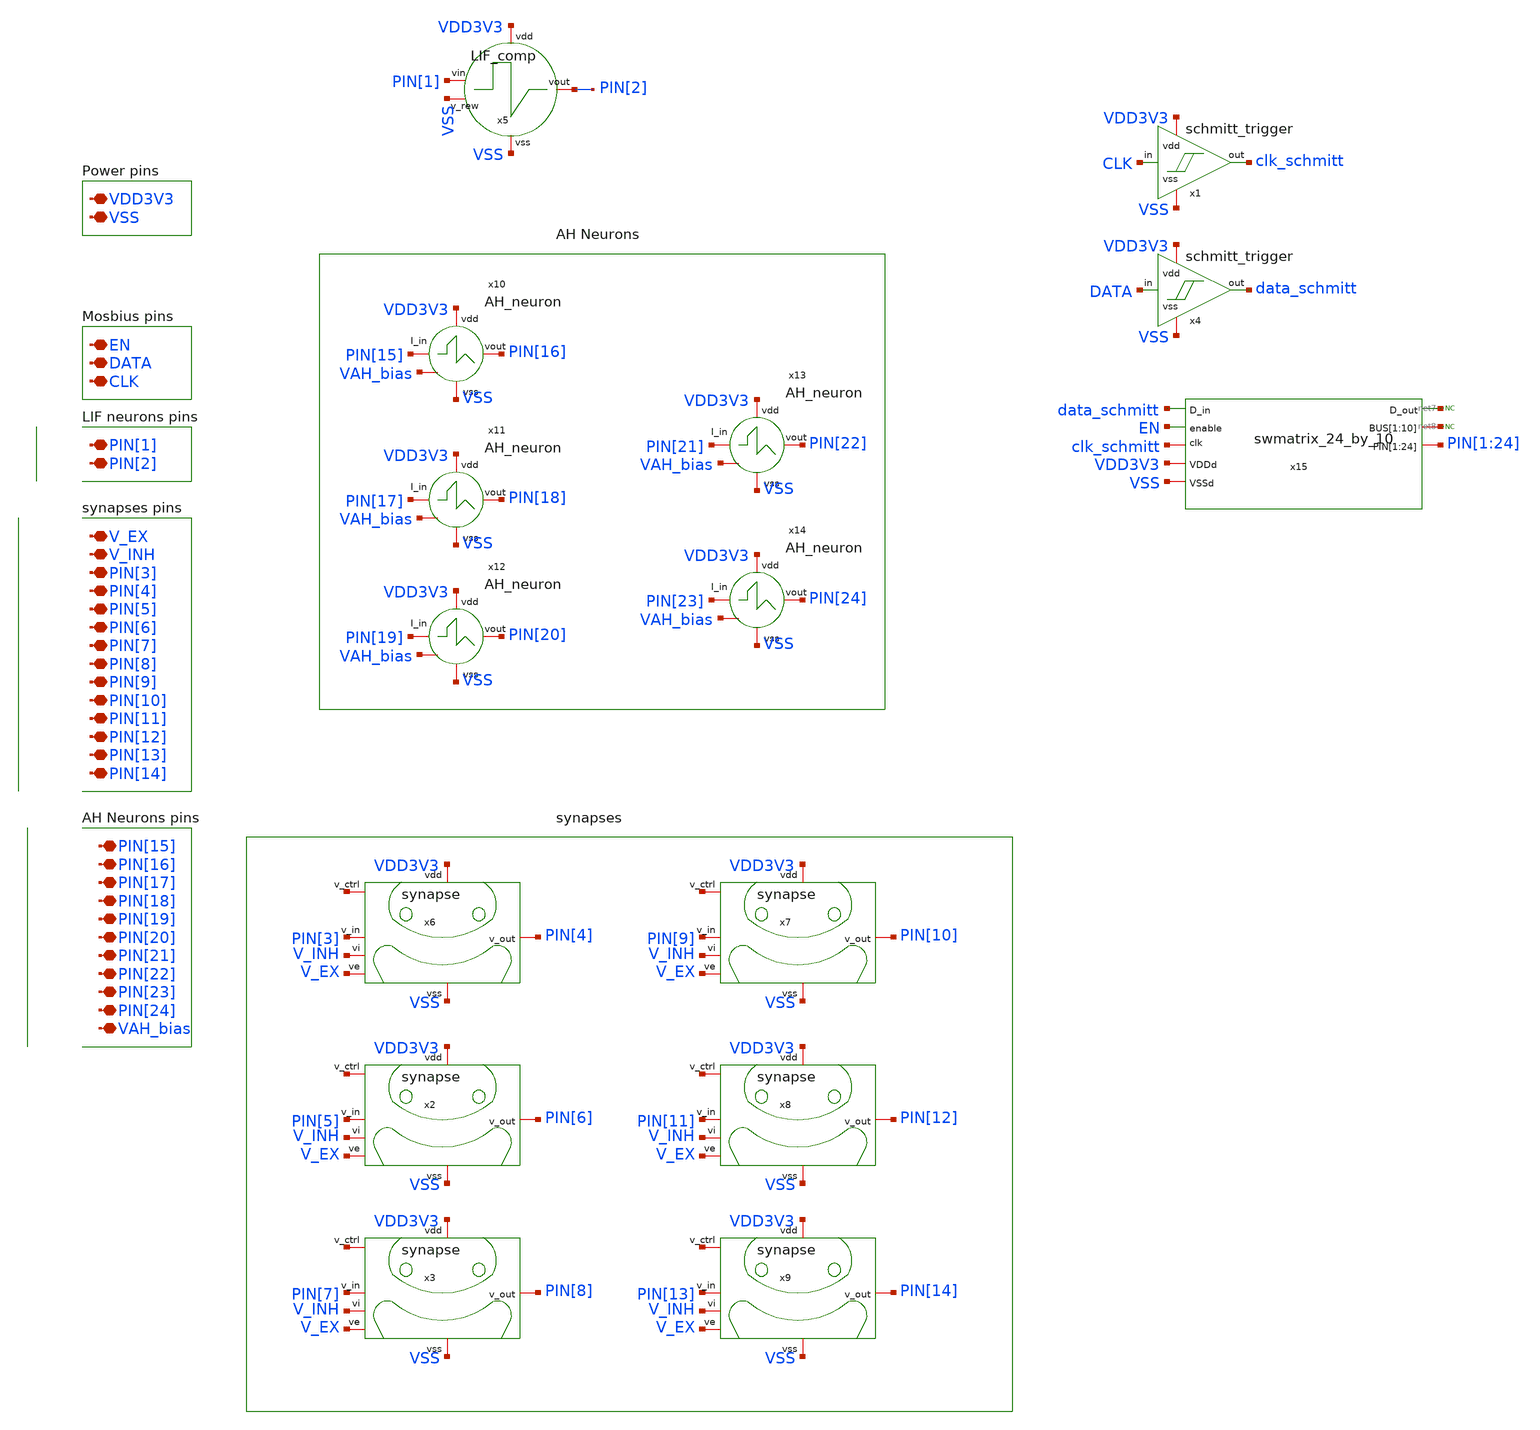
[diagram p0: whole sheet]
** sch_path: designs/klayout/layout_top/top.sch
**.subckt top PIN[15] PIN[16] PIN[17] PIN[18] PIN[19] PIN[20] PIN[21] PIN[22] VDD3V3 VSS PIN[1]
*+ PIN[2] V_EX V_INH PIN[3] PIN[4] PIN[5] PIN[6] PIN[7] PIN[8] EN DATA CLK PIN[23] PIN[24] PIN[9] PIN[10]
*+ PIN[11] PIN[12] PIN[13] PIN[14] VAH_bias
*.iopin PIN[15]
*.iopin PIN[16]
*.iopin PIN[17]
*.iopin PIN[18]
*.iopin PIN[19]
*.iopin PIN[20]
*.iopin PIN[21]
*.iopin PIN[22]
*.iopin VDD3V3
*.iopin VSS
*.iopin PIN[1]
*.iopin PIN[2]
*.iopin V_EX
*.iopin V_INH
*.iopin PIN[3]
*.iopin PIN[4]
*.iopin PIN[5]
*.iopin PIN[6]
*.iopin PIN[7]
*.iopin PIN[8]
*.iopin EN
*.iopin DATA
*.iopin CLK
*.iopin PIN[23]
*.iopin PIN[24]
*.iopin PIN[9]
*.iopin PIN[10]
*.iopin PIN[11]
*.iopin PIN[12]
*.iopin PIN[13]
*.iopin PIN[14]
*.iopin VAH_bias
x5 VDD3V3 VSS PIN[1] VSS PIN[2] LIF_comp
x6 VDD3V3 PIN[3] V_EX net1 PIN[4] V_INH VSS synapse
x2 VDD3V3 PIN[5] V_EX net2 PIN[6] V_INH VSS synapse
x3 VDD3V3 PIN[7] V_EX net3 PIN[8] V_INH VSS synapse
x7 VDD3V3 PIN[9] V_EX net4 PIN[10] V_INH VSS synapse
x8 VDD3V3 PIN[11] V_EX net5 PIN[12] V_INH VSS synapse
x9 VDD3V3 PIN[13] V_EX net6 PIN[14] V_INH VSS synapse
x10 VDD3V3 PIN[15] PIN[16] VSS VAH_bias AH_neuron
x11 VDD3V3 PIN[17] PIN[18] VSS VAH_bias AH_neuron
x12 VDD3V3 PIN[19] PIN[20] VSS VAH_bias AH_neuron
x13 VDD3V3 PIN[21] PIN[22] VSS VAH_bias AH_neuron
x14 VDD3V3 PIN[23] PIN[24] VSS VAH_bias AH_neuron
x1 clk_schmitt CLK VDD3V3 VSS schmitt_trigger
x4 data_schmitt DATA VDD3V3 VSS schmitt_trigger
x15 net7 net8 net8 net8 net8 net8 net8 net8 net8 net8 net8 PIN[1] PIN[2] PIN[3] PIN[4] PIN[5] PIN[6]
+ PIN[7] PIN[8] PIN[9] PIN[10] PIN[11] PIN[12] PIN[13] PIN[14] PIN[15] PIN[16] PIN[17] PIN[18] PIN[19]
+ PIN[20] PIN[21] PIN[22] PIN[23] PIN[24] data_schmitt VDD3V3 EN VSS clk_schmitt swmatrix_24_by_10
* noconn #net7
* noconn #net8
**.ends
.end
